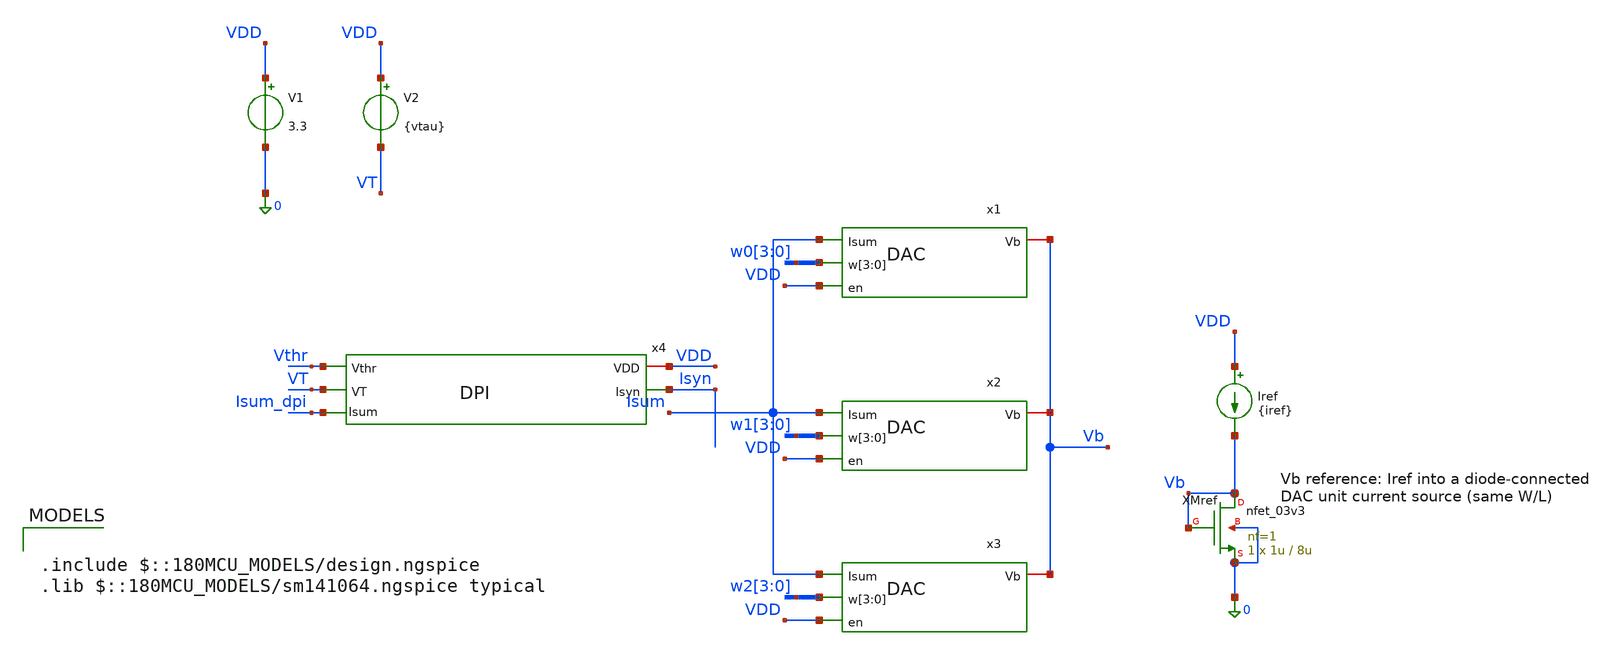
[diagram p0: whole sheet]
** sch_path: analog/neuron/DACs-DPI.sch
**.subckt DACs-DPI
x1 Isum Vb w0[3] w0[2] w0[1] w0[0] VDD DAC
x2 Isum Vb w1[3] w1[2] w1[1] w1[0] VDD DAC
x3 Isum Vb w2[3] w2[2] w2[1] w2[0] VDD DAC
x4 VDD Vthr Isyn Isum_dpi VT DPI
Iref VDD Vb {iref}
XMref Vb Vb 0 0 nfet_03v3 L=8u W=1u nf=1 ad='int((nf+1)/2) * W/nf * 0.18u' as='int((nf+2)/2) * W/nf * 0.18u'
+ pd='2*int((nf+1)/2) * (W/nf + 0.18u)' ps='2*int((nf+2)/2) * (W/nf + 0.18u)' nrd='0.18u / W' nrs='0.18u / W'
+ sa=0 sb=0 sd=0 m=1
V1 VDD 0 3.3
V2 VDD VT {vtau}
**** begin user architecture code

.include $::180MCU_MODELS/design.ngspice
.lib $::180MCU_MODELS/sm141064.ngspice typical



* DAC + DPI weight-code test.
* One input spike of width tpw every tsp, starting at t0. Spike k (k = 0..15)
* carries code k: bit b of k drives w<d>[b] of DAC x<d+1> while the spike is high.
* d1, d2, d3 = 1 send the codes to x1, x2, x3 (default: x1 only).
* DAC branch weights w[0]..w[3] = 1:2:3:4; iref sets the unit (w[0]) current,
* trimmed so that w[0] gives 15 nA here (the mirror reads about 4 % high, because
* V(Isum) ~ 2.5 V while the diode sits at ~0.6 V).
* DPI biases from analog/testbenches/README.md (before: Vthr = 3 V, VDD - VT = 0.5 V).
.param vdd=3.3 vthr=2.9 vtau=0.40 iref=14.42n tpw=10u tsp=2m t0=1m d1=1 d2=0 d3=0
.csparam tpw_c={tpw}
.csparam tsp_c={tsp}
.csparam t0_c={t0}

Vthr  Vthr 0 {vthr}
VIdac Isum_dpi Isum 0
VIsyn Isyn 0 0

* Spike train, and one gate per code bit: gate b is high around the spikes k
* whose bit b is set (delay (2^b - 0.5) tsp, width 2^b tsp, period 2^(b+1) tsp)
Vspk spk 0 pulse(0 1 {t0} 10n 10n {tpw} {tsp})
Vg0 g0 0 pulse(0 1 {t0+0.5*tsp} 10n 10n {tsp} {2*tsp})
Vg1 g1 0 pulse(0 1 {t0+1.5*tsp} 10n 10n {2*tsp} {4*tsp})
Vg2 g2 0 pulse(0 1 {t0+3.5*tsp} 10n 10n {4*tsp} {8*tsp})
Vg3 g3 0 pulse(0 1 {t0+7.5*tsp} 10n 10n {8*tsp} {16*tsp})

* Bw<b><d> drives bit <b> of DAC x<d+1>, net w<d>[<b>]
Bw00 w0[0] 0 V = vdd*d1*v(spk)*v(g0)
Bw10 w0[1] 0 V = vdd*d1*v(spk)*v(g1)
Bw20 w0[2] 0 V = vdd*d1*v(spk)*v(g2)
Bw30 w0[3] 0 V = vdd*d1*v(spk)*v(g3)
Bw01 w1[0] 0 V = vdd*d2*v(spk)*v(g0)
Bw11 w1[1] 0 V = vdd*d2*v(spk)*v(g1)
Bw21 w1[2] 0 V = vdd*d2*v(spk)*v(g2)
Bw31 w1[3] 0 V = vdd*d2*v(spk)*v(g3)
Bw02 w2[0] 0 V = vdd*d3*v(spk)*v(g0)
Bw12 w2[1] 0 V = vdd*d3*v(spk)*v(g1)
Bw22 w2[2] 0 V = vdd*d3*v(spk)*v(g2)
Bw32 w2[3] 0 V = vdd*d3*v(spk)*v(g3)

.control
  save all
  set wr_singlescale
  set wr_vecnames
  tran 0.1u 33.5m 0 1u
  let idac = i(VIdac)
  let isyn = i(VIsyn)
  * Ideal weight of each code with branch weights 1:2:3:4
  compose wsum values 0 1 2 3 3 4 5 6 4 5 6 7 7 8 9 10

  * Per spike window k: DAC current while the spike is high (second half of the
  * spike), DAC leakage between spikes, charge per spike with the leakage
  * removed, and the DPI output peak. Unit = code 1 (w[0] only).
  let ion = vector(16)
  let leak = vector(16)
  let qnet = vector(16)
  let ipk = vector(16)
  let k = 0
  while k < 16
    let ts = t0_c + k*tsp_c
    let ta = ts + 0.5*tpw_c
    let tb = ts + 0.95*tpw_c
    let tl = ts + 0.5*tsp_c
    let te = ts + tsp_c - 1u
    meas tran m_on avg idac from=$&ta to=$&tb
    meas tran m_leak avg idac from=$&tl to=$&te
    meas tran m_q integ idac from=$&ts to=$&te
    meas tran m_pk max isyn from=$&ts to=$&te
    let ion[k] = m_on - m_leak
    let leak[k] = m_leak
    let qnet[k] = m_q - m_leak*(te - ts)
    let ipk[k] = m_pk
    let k = k + 1
  end

  let iunit = ion[1]
  echo
  echo code  weight  Idac(nA)  Idac/unit  error  Qnet(pC)  Isyn_peak(nA)
  let errmax = 0
  let k = 0
  while k < 16
    let wk = wsum[k]
    let ratio = ion[k]/iunit
    let err = 0
    if k > 0
      let err = ratio/wk - 1
      if abs(err) > errmax
        let errmax = abs(err)
      end
    end
    let ion_na = ion[k]*1e9
    let q_pc = qnet[k]*1e12
    let ipk_na = ipk[k]*1e9
    echo $&k  $&wk  $&ion_na  $&ratio  $&err  $&q_pc  $&ipk_na
    let k = k + 1
  end
  let k = 0
  while k < 16
    let v1 = ion[k]
    let v2 = qnet[k]
    let v3 = ipk[k]
    echo RES idac_$&k=$&v1
    echo RES q_$&k=$&v2
    echo RES isyn_pk_$&k=$&v3
    let k = k + 1
  end
  let v1 = leak[0]
  echo RES iunit=$&iunit
  echo RES idac_leak=$&v1
  echo RES dac_err_max=$&errmax

  wrdata dacs_dpi_codes.txt idac isyn
  if $?batchmode = 0
    plot idac title 'DAC output current (code k on spike k)' ylabel 'A'
    plot isyn title 'DPI output current' ylabel 'A'
    plot v(w0[0]) v(w0[1])+4 v(w0[2])+8 v(w0[3])+12 title 'x1 weight bits'
  end
.endc


**** end user architecture code
**.ends

* expanding   symbol:  DAC.sym # of pins=4
** sym_path: analog/neuron/DAC.sym
** sch_path: analog/neuron/DAC.sch
.subckt DAC Isum Vb w[3] w[2] w[1] w[0] en
*.iopin Vb
*.ipin w[3],w[2],w[1],w[0]
*.ipin Isum
*.ipin en
XM1 X w[0] net4 net4 nfet_03v3 L=0.28u W=0.22u nf=1 ad='int((nf+1)/2) * W/nf * 0.18u' as='int((nf+2)/2) * W/nf * 0.18u'
+ pd='2*int((nf+1)/2) * (W/nf + 0.18u)' ps='2*int((nf+2)/2) * (W/nf + 0.18u)' nrd='0.18u / W' nrs='0.18u / W'
+ sa=0 sb=0 sd=0 m=1
XM2 net4 Vb GND GND nfet_03v3 L=8u W=1u nf=1 ad='int((nf+1)/2) * W/nf * 0.18u' as='int((nf+2)/2) * W/nf * 0.18u'
+ pd='2*int((nf+1)/2) * (W/nf + 0.18u)' ps='2*int((nf+2)/2) * (W/nf + 0.18u)' nrd='0.18u / W' nrs='0.18u / W'
+ sa=0 sb=0 sd=0 m=1
XM3 X w[1] net2 net2 nfet_03v3 L=0.28u W=0.22u nf=1 ad='int((nf+1)/2) * W/nf * 0.18u' as='int((nf+2)/2) * W/nf * 0.18u'
+ pd='2*int((nf+1)/2) * (W/nf + 0.18u)' ps='2*int((nf+2)/2) * (W/nf + 0.18u)' nrd='0.18u / W' nrs='0.18u / W'
+ sa=0 sb=0 sd=0 m=2
XM4 net2 Vb GND GND nfet_03v3 L=8u W=1u nf=1 ad='int((nf+1)/2) * W/nf * 0.18u' as='int((nf+2)/2) * W/nf * 0.18u'
+ pd='2*int((nf+1)/2) * (W/nf + 0.18u)' ps='2*int((nf+2)/2) * (W/nf + 0.18u)' nrd='0.18u / W' nrs='0.18u / W'
+ sa=0 sb=0 sd=0 m=2
XM5 X w[2] net3 net3 nfet_03v3 L=0.28u W=0.22u nf=1 ad='int((nf+1)/2) * W/nf * 0.18u' as='int((nf+2)/2) * W/nf * 0.18u'
+ pd='2*int((nf+1)/2) * (W/nf + 0.18u)' ps='2*int((nf+2)/2) * (W/nf + 0.18u)' nrd='0.18u / W' nrs='0.18u / W'
+ sa=0 sb=0 sd=0 m=3
XM6 net3 Vb GND GND nfet_03v3 L=8u W=1u nf=1 ad='int((nf+1)/2) * W/nf * 0.18u' as='int((nf+2)/2) * W/nf * 0.18u'
+ pd='2*int((nf+1)/2) * (W/nf + 0.18u)' ps='2*int((nf+2)/2) * (W/nf + 0.18u)' nrd='0.18u / W' nrs='0.18u / W'
+ sa=0 sb=0 sd=0 m=3
XM7 X w[3] net1 net1 nfet_03v3 L=0.28u W=0.22u nf=1 ad='int((nf+1)/2) * W/nf * 0.18u' as='int((nf+2)/2) * W/nf * 0.18u'
+ pd='2*int((nf+1)/2) * (W/nf + 0.18u)' ps='2*int((nf+2)/2) * (W/nf + 0.18u)' nrd='0.18u / W' nrs='0.18u / W'
+ sa=0 sb=0 sd=0 m=4
XM8 net1 Vb GND GND nfet_03v3 L=8u W=1u nf=1 ad='int((nf+1)/2) * W/nf * 0.18u' as='int((nf+2)/2) * W/nf * 0.18u'
+ pd='2*int((nf+1)/2) * (W/nf + 0.18u)' ps='2*int((nf+2)/2) * (W/nf + 0.18u)' nrd='0.18u / W' nrs='0.18u / W'
+ sa=0 sb=0 sd=0 m=4
XMen Isum en X GND nfet_03v3 L=0.28u W=0.22u nf=1 ad='int((nf+1)/2) * W/nf * 0.18u' as='int((nf+2)/2) * W/nf * 0.18u'
+ pd='2*int((nf+1)/2) * (W/nf + 0.18u)' ps='2*int((nf+2)/2) * (W/nf + 0.18u)' nrd='0.18u / W' nrs='0.18u / W'
+ sa=0 sb=0 sd=0 m=1
.ends


* expanding   symbol:  DPI.sym # of pins=5
** sym_path: analog/neuron/DPI.sym
** sch_path: analog/neuron/DPI.sch
.subckt DPI VDD Vthr Isyn Isum VT
*.ipin Vthr
*.iopin VDD
*.opin Isyn
*.opin Isum
*.ipin VT
XM1 VDD Vthr Isum Isum nfet_03v3 L=0.28u W=0.22u nf=1 ad='int((nf+1)/2) * W/nf * 0.18u' as='int((nf+2)/2) * W/nf * 0.18u'
+ pd='2*int((nf+1)/2) * (W/nf + 0.18u)' ps='2*int((nf+2)/2) * (W/nf + 0.18u)' nrd='0.18u / W' nrs='0.18u / W'
+ sa=0 sb=0 sd=0 m=1
XM2 net1 net1 Isum Isum nfet_03v3 L=0.28u W=0.22u nf=1 ad='int((nf+1)/2) * W/nf * 0.18u' as='int((nf+2)/2) * W/nf * 0.18u'
+ pd='2*int((nf+1)/2) * (W/nf + 0.18u)' ps='2*int((nf+2)/2) * (W/nf + 0.18u)' nrd='0.18u / W' nrs='0.18u / W'
+ sa=0 sb=0 sd=0 m=1
XM3 net1 VT VDD VDD pfet_03v3 L=0.28u W=0.22u nf=1 ad='int((nf+1)/2) * W/nf * 0.18u' as='int((nf+2)/2) * W/nf * 0.18u'
+ pd='2*int((nf+1)/2) * (W/nf + 0.18u)' ps='2*int((nf+2)/2) * (W/nf + 0.18u)' nrd='0.18u / W' nrs='0.18u / W'
+ sa=0 sb=0 sd=0 m=1
XM4 Isyn net1 VDD VDD pfet_03v3 L=0.28u W=0.22u nf=1 ad='int((nf+1)/2) * W/nf * 0.18u' as='int((nf+2)/2) * W/nf * 0.18u'
+ pd='2*int((nf+1)/2) * (W/nf + 0.18u)' ps='2*int((nf+2)/2) * (W/nf + 0.18u)' nrd='0.18u / W' nrs='0.18u / W'
+ sa=0 sb=0 sd=0 m=1
C4 VDD net1 1p m=1
.ends

.GLOBAL GND
.end
